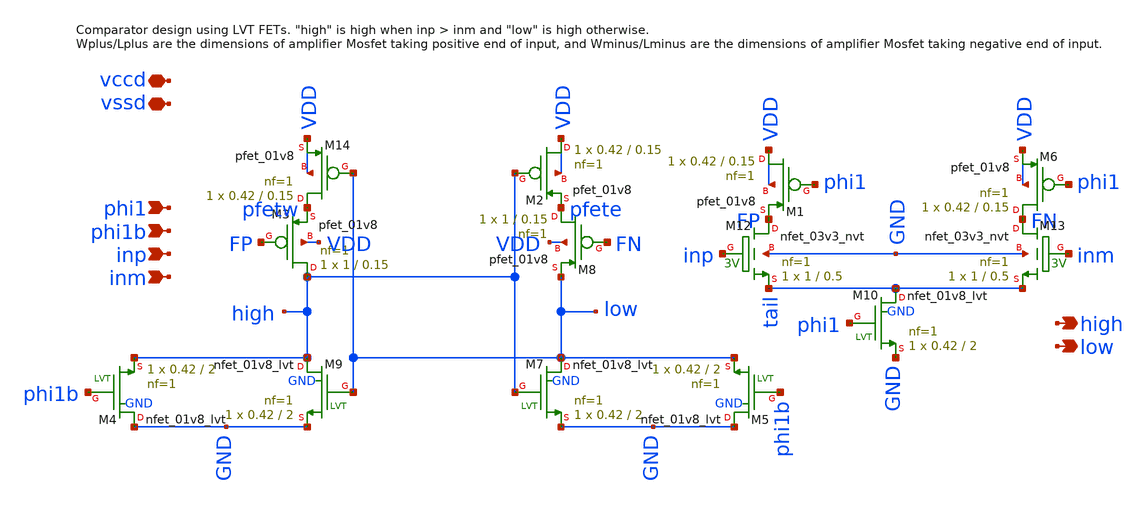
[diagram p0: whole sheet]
** sch_path: xschem/comparator_latest/comparator_single_tail.sch
**.subckt comparator_single_tail phi1 high phi1b inp inm low vccd vssd
*.ipin phi1
*.opin high
*.ipin phi1b
*.ipin inp
*.ipin inm
*.opin low
*.iopin vccd
*.iopin vssd
XM12 FP inp tail GND sky130_fd_pr__nfet_03v3_nvt L=0.5 W=1 nf=1 ad='int((nf+1)/2) * W/nf * 0.29' as='int((nf+2)/2) * W/nf * 0.29'
+ pd='2*int((nf+1)/2) * (W/nf + 0.29)' ps='2*int((nf+2)/2) * (W/nf + 0.29)' nrd='0.29 / W' nrs='0.29 / W'
+ sa=0 sb=0 sd=0 mult=1 m=1
XM13 FN inm tail GND sky130_fd_pr__nfet_03v3_nvt L=0.5 W=1 nf=1 ad='int((nf+1)/2) * W/nf * 0.29' as='int((nf+2)/2) * W/nf * 0.29'
+ pd='2*int((nf+1)/2) * (W/nf + 0.29)' ps='2*int((nf+2)/2) * (W/nf + 0.29)' nrd='0.29 / W' nrs='0.29 / W'
+ sa=0 sb=0 sd=0 mult=1 m=1
XM14 pfetw low VDD VDD sky130_fd_pr__pfet_01v8 L=0.15 W=0.42 nf=1 ad='int((nf+1)/2) * W/nf * 0.29' as='int((nf+2)/2) * W/nf * 0.29'
+ pd='2*int((nf+1)/2) * (W/nf + 0.29)' ps='2*int((nf+2)/2) * (W/nf + 0.29)' nrd='0.29 / W' nrs='0.29 / W'
+ sa=0 sb=0 sd=0 mult=1 m=1
XM3 high FP pfetw VDD sky130_fd_pr__pfet_01v8 L=0.15 W=1 nf=1 ad='int((nf+1)/2) * W/nf * 0.29' as='int((nf+2)/2) * W/nf * 0.29'
+ pd='2*int((nf+1)/2) * (W/nf + 0.29)' ps='2*int((nf+2)/2) * (W/nf + 0.29)' nrd='0.29 / W' nrs='0.29 / W'
+ sa=0 sb=0 sd=0 mult=1 m=1
XM8 pfete FN low VDD sky130_fd_pr__pfet_01v8 L=0.15 W=1 nf=1 ad='int((nf+1)/2) * W/nf * 0.29' as='int((nf+2)/2) * W/nf * 0.29'
+ pd='2*int((nf+1)/2) * (W/nf + 0.29)' ps='2*int((nf+2)/2) * (W/nf + 0.29)' nrd='0.29 / W' nrs='0.29 / W'
+ sa=0 sb=0 sd=0 mult=1 m=1
XM2 VDD high pfete VDD sky130_fd_pr__pfet_01v8 L=0.15 W=0.42 nf=1 ad='int((nf+1)/2) * W/nf * 0.29' as='int((nf+2)/2) * W/nf * 0.29'
+ pd='2*int((nf+1)/2) * (W/nf + 0.29)' ps='2*int((nf+2)/2) * (W/nf + 0.29)' nrd='0.29 / W' nrs='0.29 / W'
+ sa=0 sb=0 sd=0 mult=1 m=1
XM5 GND phi1b low GND sky130_fd_pr__nfet_01v8_lvt L=2 W=0.42 nf=1 ad='int((nf+1)/2) * W/nf * 0.29' as='int((nf+2)/2) * W/nf * 0.29'
+ pd='2*int((nf+1)/2) * (W/nf + 0.29)' ps='2*int((nf+2)/2) * (W/nf + 0.29)' nrd='0.29 / W' nrs='0.29 / W'
+ sa=0 sb=0 sd=0 mult=1 m=1
XM4 GND phi1b high GND sky130_fd_pr__nfet_01v8_lvt L=2 W=0.42 nf=1 ad='int((nf+1)/2) * W/nf * 0.29' as='int((nf+2)/2) * W/nf * 0.29'
+ pd='2*int((nf+1)/2) * (W/nf + 0.29)' ps='2*int((nf+2)/2) * (W/nf + 0.29)' nrd='0.29 / W' nrs='0.29 / W'
+ sa=0 sb=0 sd=0 mult=1 m=1
XM7 low high GND GND sky130_fd_pr__nfet_01v8_lvt L=2 W=0.42 nf=1 ad='int((nf+1)/2) * W/nf * 0.29' as='int((nf+2)/2) * W/nf * 0.29'
+ pd='2*int((nf+1)/2) * (W/nf + 0.29)' ps='2*int((nf+2)/2) * (W/nf + 0.29)' nrd='0.29 / W' nrs='0.29 / W'
+ sa=0 sb=0 sd=0 mult=1 m=1
XM9 high low GND GND sky130_fd_pr__nfet_01v8_lvt L=2 W=0.42 nf=1 ad='int((nf+1)/2) * W/nf * 0.29' as='int((nf+2)/2) * W/nf * 0.29'
+ pd='2*int((nf+1)/2) * (W/nf + 0.29)' ps='2*int((nf+2)/2) * (W/nf + 0.29)' nrd='0.29 / W' nrs='0.29 / W'
+ sa=0 sb=0 sd=0 mult=1 m=1
XM10 tail phi1 GND GND sky130_fd_pr__nfet_01v8_lvt L=2 W=0.42 nf=1 ad='int((nf+1)/2) * W/nf * 0.29' as='int((nf+2)/2) * W/nf * 0.29'
+ pd='2*int((nf+1)/2) * (W/nf + 0.29)' ps='2*int((nf+2)/2) * (W/nf + 0.29)' nrd='0.29 / W' nrs='0.29 / W'
+ sa=0 sb=0 sd=0 mult=1 m=1
XM1 VDD phi1 FP VDD sky130_fd_pr__pfet_01v8 L=0.15 W=0.42 nf=1 ad='int((nf+1)/2) * W/nf * 0.29' as='int((nf+2)/2) * W/nf * 0.29'
+ pd='2*int((nf+1)/2) * (W/nf + 0.29)' ps='2*int((nf+2)/2) * (W/nf + 0.29)' nrd='0.29 / W' nrs='0.29 / W'
+ sa=0 sb=0 sd=0 mult=1 m=1
XM6 FN phi1 VDD VDD sky130_fd_pr__pfet_01v8 L=0.15 W=0.42 nf=1 ad='int((nf+1)/2) * W/nf * 0.29' as='int((nf+2)/2) * W/nf * 0.29'
+ pd='2*int((nf+1)/2) * (W/nf + 0.29)' ps='2*int((nf+2)/2) * (W/nf + 0.29)' nrd='0.29 / W' nrs='0.29 / W'
+ sa=0 sb=0 sd=0 mult=1 m=1
**.ends
.end
